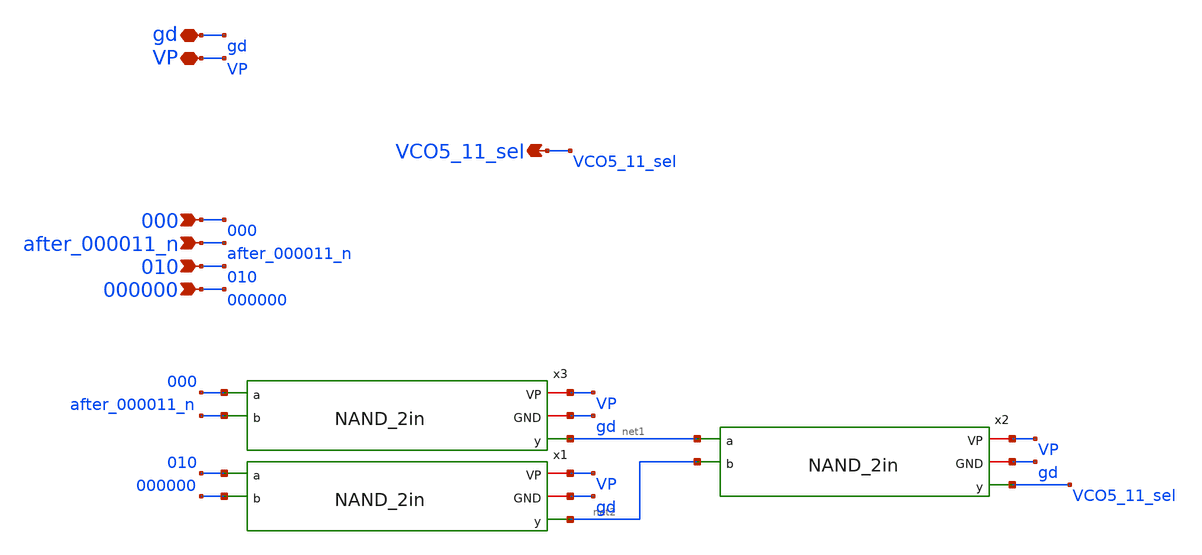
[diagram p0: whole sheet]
** sch_path: schematics/divider/schematics/VCO5_selection.sch
**.subckt VCO5_selection gd VP VCO5_11_sel 000 after_000011_n 010 000000
*.iopin gd
*.iopin VP
*.opin VCO5_11_sel
*.ipin 000
*.ipin after_000011_n
*.ipin 010
*.ipin 000000
x1 VP gd 010 net2 000000 NAND_2in
x2 VP gd net1 VCO5_11_sel net2 NAND_2in
x3 VP gd 000 net1 after_000011_n NAND_2in
**.ends

* expanding   symbol:  NAND_2in.sym # of pins=5
** sym_path: schematics/divider/schematics/NAND_2in.sym
** sch_path: schematics/divider/schematics/NAND_2in.sch
.subckt NAND_2in VP GND a y b
*.opin y
*.iopin GND
*.ipin a
*.iopin VP
*.ipin b
XM1 y a net1 GND sg13_lv_nmos w=0.15u l=0.13u ng=1 m=1 mm_ok=1
XM3 net1 b GND GND sg13_lv_nmos w=0.15u l=0.13u ng=1 m=1 mm_ok=1
XM2 y b VP VP sg13_lv_pmos w=0.15u l=0.13u ng=1 m=1 mm_ok=1
XM4 y a VP VP sg13_lv_pmos w=0.15u l=0.13u ng=1 m=1 mm_ok=1
.ends

.end
